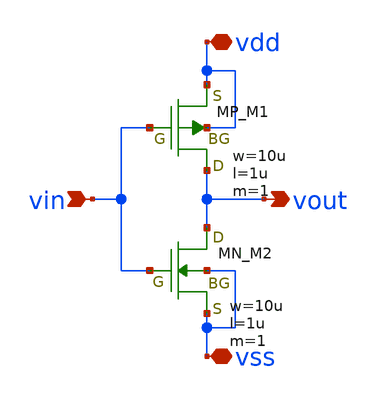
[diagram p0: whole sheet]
** sch_path: member_project/Tiny555/yamada3/xschem/inverter_15v.sch
**.subckt inverter_15v vin vdd vss vout
*.ipin vin
*.iopin vdd
*.iopin vss
*.opin vout
XM1 vout vin vdd vdd PMOS w=10u l=1u as=0 ad=0 ps=0 pd=0 nrd=0 nrs=0 m=1
XM2 vout vin vss vss NMOS w=10u l=1u as=0 ad=0 ps=0 pd=0 nrd=0 nrs=0 m=1
**.ends
.end
